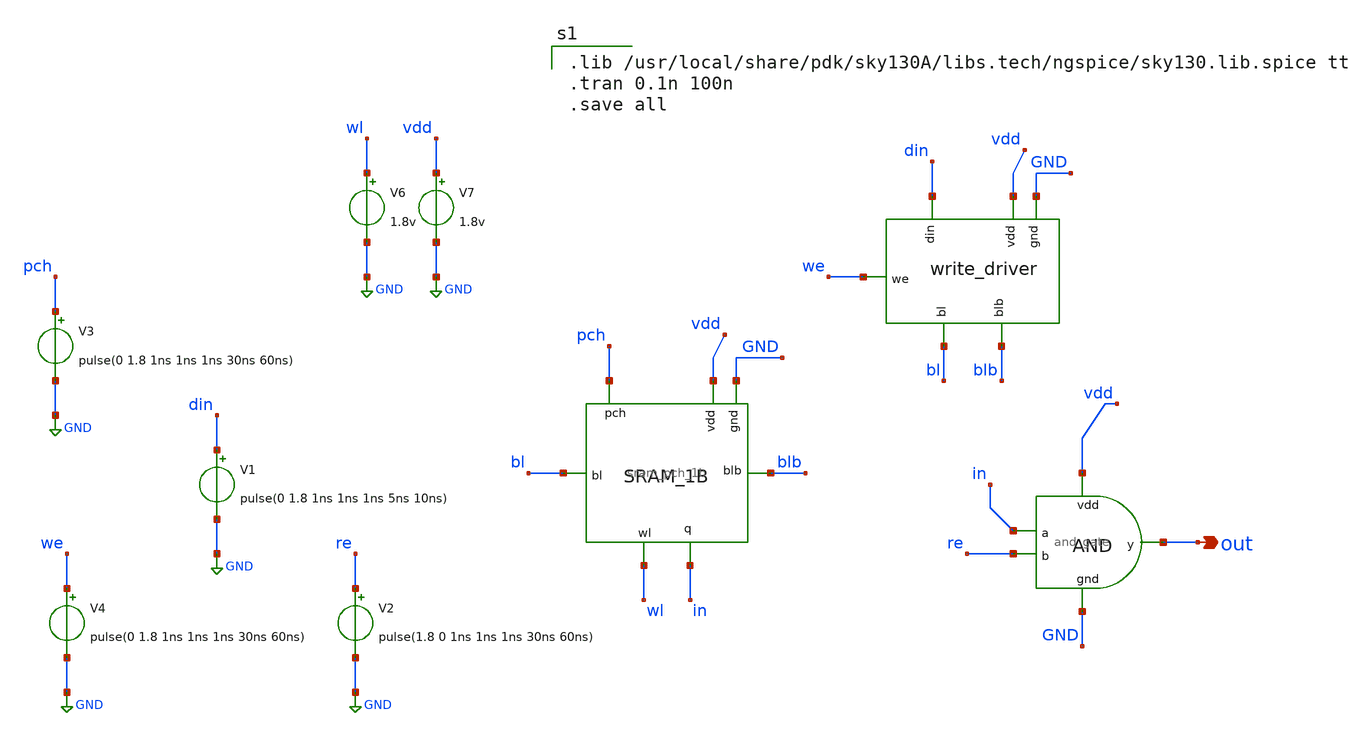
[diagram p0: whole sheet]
** sch_path: sram/sram1b_tb.sch
**.subckt sram1b_tb out
*.opin out
V1 din GND pulse(0 1.8 1ns 1ns 1ns 5ns 10ns)
V6 wl GND 1.8v
V7 vdd GND 1.8v
x2 vdd GND din bl blb we write_driver
x1 pch wl bl in GND vdd blb sram_pch_1b
V2 re GND pulse(1.8 0 1ns 1ns 1ns 30ns 60ns)
V4 we GND pulse(0 1.8 1ns 1ns 1ns 30ns 60ns)
V3 pch GND pulse(0 1.8 1ns 1ns 1ns 30ns 60ns)
x3 vdd in out re GND and_gate
**** begin user architecture code

.lib /usr/local/share/pdk/sky130A/libs.tech/ngspice/sky130.lib.spice tt
.tran 0.1n 100n
.save all

**** end user architecture code
**.ends

* expanding   symbol:  write_driver.sym # of pins=6
** sym_path: sram/write_driver.sym
** sch_path: sram/write_driver.sch
.subckt write_driver vdd gnd din bl blb we
*.ipin din
*.ipin we
*.opin bl
*.opin blb
*.ipin vdd
*.ipin gnd
XM1 net2 web vdd vdd sky130_fd_pr__pfet_01v8 L=0.15 W=1 nf=1 ad='int((nf+1)/2) * W/nf * 0.29' as='int((nf+2)/2) * W/nf * 0.29'
+ pd='2*int((nf+1)/2) * (W/nf + 0.29)' ps='2*int((nf+2)/2) * (W/nf + 0.29)' nrd='0.29 / W' nrs='0.29 / W'
+ sa=0 sb=0 sd=0 mult=1 m=1
XM2 blb din net1 blb sky130_fd_pr__nfet_01v8 L=0.15 W=1 nf=1 ad='int((nf+1)/2) * W/nf * 0.29' as='int((nf+2)/2) * W/nf * 0.29'
+ pd='2*int((nf+1)/2) * (W/nf + 0.29)' ps='2*int((nf+2)/2) * (W/nf + 0.29)' nrd='0.29 / W' nrs='0.29 / W'
+ sa=0 sb=0 sd=0 mult=1 m=1
XM3 blb din net2 net2 sky130_fd_pr__pfet_01v8 L=0.15 W=1 nf=1 ad='int((nf+1)/2) * W/nf * 0.29' as='int((nf+2)/2) * W/nf * 0.29'
+ pd='2*int((nf+1)/2) * (W/nf + 0.29)' ps='2*int((nf+2)/2) * (W/nf + 0.29)' nrd='0.29 / W' nrs='0.29 / W'
+ sa=0 sb=0 sd=0 mult=1 m=1
XM4 net1 we gnd net1 sky130_fd_pr__nfet_01v8 L=0.15 W=1 nf=1 ad='int((nf+1)/2) * W/nf * 0.29' as='int((nf+2)/2) * W/nf * 0.29'
+ pd='2*int((nf+1)/2) * (W/nf + 0.29)' ps='2*int((nf+2)/2) * (W/nf + 0.29)' nrd='0.29 / W' nrs='0.29 / W'
+ sa=0 sb=0 sd=0 mult=1 m=1
XM5 net4 web vdd vdd sky130_fd_pr__pfet_01v8 L=0.15 W=1 nf=1 ad='int((nf+1)/2) * W/nf * 0.29' as='int((nf+2)/2) * W/nf * 0.29'
+ pd='2*int((nf+1)/2) * (W/nf + 0.29)' ps='2*int((nf+2)/2) * (W/nf + 0.29)' nrd='0.29 / W' nrs='0.29 / W'
+ sa=0 sb=0 sd=0 mult=1 m=1
XM6 bl dinb net3 net3 sky130_fd_pr__nfet_01v8 L=0.15 W=1 nf=1 ad='int((nf+1)/2) * W/nf * 0.29' as='int((nf+2)/2) * W/nf * 0.29'
+ pd='2*int((nf+1)/2) * (W/nf + 0.29)' ps='2*int((nf+2)/2) * (W/nf + 0.29)' nrd='0.29 / W' nrs='0.29 / W'
+ sa=0 sb=0 sd=0 mult=1 m=1
XM7 bl dinb net4 net4 sky130_fd_pr__pfet_01v8 L=0.15 W=1 nf=1 ad='int((nf+1)/2) * W/nf * 0.29' as='int((nf+2)/2) * W/nf * 0.29'
+ pd='2*int((nf+1)/2) * (W/nf + 0.29)' ps='2*int((nf+2)/2) * (W/nf + 0.29)' nrd='0.29 / W' nrs='0.29 / W'
+ sa=0 sb=0 sd=0 mult=1 m=1
XM8 net3 we gnd gnd sky130_fd_pr__nfet_01v8 L=0.15 W=1 nf=1 ad='int((nf+1)/2) * W/nf * 0.29' as='int((nf+2)/2) * W/nf * 0.29'
+ pd='2*int((nf+1)/2) * (W/nf + 0.29)' ps='2*int((nf+2)/2) * (W/nf + 0.29)' nrd='0.29 / W' nrs='0.29 / W'
+ sa=0 sb=0 sd=0 mult=1 m=1
x1 vdd din dinb gnd inverter
x2 vdd we web gnd inverter
.ends


* expanding   symbol:  sram_pch_1b.sym # of pins=7
** sym_path: sram/sram_pch_1b.sym
** sch_path: sram/sram_pch_1b.sch
.subckt sram_pch_1b pch wl bl q gnd vdd blb
*.ipin gnd
*.ipin bl
*.ipin blb
*.ipin vdd
*.ipin wl
*.ipin pch
*.opin q
XM1 blb wl net1 gnd sky130_fd_pr__nfet_01v8 L=0.15 W=1 nf=1 ad='int((nf+1)/2) * W/nf * 0.29' as='int((nf+2)/2) * W/nf * 0.29'
+ pd='2*int((nf+1)/2) * (W/nf + 0.29)' ps='2*int((nf+2)/2) * (W/nf + 0.29)' nrd='0.29 / W' nrs='0.29 / W'
+ sa=0 sb=0 sd=0 mult=1 m=1
XM3 q wl bl gnd sky130_fd_pr__nfet_01v8 L=0.15 W=1 nf=1 ad='int((nf+1)/2) * W/nf * 0.29' as='int((nf+2)/2) * W/nf * 0.29'
+ pd='2*int((nf+1)/2) * (W/nf + 0.29)' ps='2*int((nf+2)/2) * (W/nf + 0.29)' nrd='0.29 / W' nrs='0.29 / W'
+ sa=0 sb=0 sd=0 mult=1 m=1
XM5 q net1 vdd vdd sky130_fd_pr__pfet_01v8 L=0.15 W=1 nf=1 ad='int((nf+1)/2) * W/nf * 0.29' as='int((nf+2)/2) * W/nf * 0.29'
+ pd='2*int((nf+1)/2) * (W/nf + 0.29)' ps='2*int((nf+2)/2) * (W/nf + 0.29)' nrd='0.29 / W' nrs='0.29 / W'
+ sa=0 sb=0 sd=0 mult=1 m=1
XM6 net1 q vdd vdd sky130_fd_pr__pfet_01v8 L=0.15 W=1 nf=1 ad='int((nf+1)/2) * W/nf * 0.29' as='int((nf+2)/2) * W/nf * 0.29'
+ pd='2*int((nf+1)/2) * (W/nf + 0.29)' ps='2*int((nf+2)/2) * (W/nf + 0.29)' nrd='0.29 / W' nrs='0.29 / W'
+ sa=0 sb=0 sd=0 mult=1 m=1
XM7 bl pch vdd vdd sky130_fd_pr__pfet_01v8 L=0.15 W=1 nf=1 ad='int((nf+1)/2) * W/nf * 0.29' as='int((nf+2)/2) * W/nf * 0.29'
+ pd='2*int((nf+1)/2) * (W/nf + 0.29)' ps='2*int((nf+2)/2) * (W/nf + 0.29)' nrd='0.29 / W' nrs='0.29 / W'
+ sa=0 sb=0 sd=0 mult=1 m=1
XM8 blb pch vdd vdd sky130_fd_pr__pfet_01v8 L=0.15 W=1 nf=1 ad='int((nf+1)/2) * W/nf * 0.29' as='int((nf+2)/2) * W/nf * 0.29'
+ pd='2*int((nf+1)/2) * (W/nf + 0.29)' ps='2*int((nf+2)/2) * (W/nf + 0.29)' nrd='0.29 / W' nrs='0.29 / W'
+ sa=0 sb=0 sd=0 mult=1 m=1
XM9 bl pch blb blb sky130_fd_pr__pfet_01v8 L=0.15 W=1 nf=1 ad='int((nf+1)/2) * W/nf * 0.29' as='int((nf+2)/2) * W/nf * 0.29'
+ pd='2*int((nf+1)/2) * (W/nf + 0.29)' ps='2*int((nf+2)/2) * (W/nf + 0.29)' nrd='0.29 / W' nrs='0.29 / W'
+ sa=0 sb=0 sd=0 mult=1 m=1
XM2 net1 q gnd gnd sky130_fd_pr__nfet_01v8 L=0.15 W=1 nf=1 ad='int((nf+1)/2) * W/nf * 0.29' as='int((nf+2)/2) * W/nf * 0.29'
+ pd='2*int((nf+1)/2) * (W/nf + 0.29)' ps='2*int((nf+2)/2) * (W/nf + 0.29)' nrd='0.29 / W' nrs='0.29 / W'
+ sa=0 sb=0 sd=0 mult=1 m=1
XM4 q net1 gnd gnd sky130_fd_pr__nfet_01v8 L=0.15 W=1 nf=1 ad='int((nf+1)/2) * W/nf * 0.29' as='int((nf+2)/2) * W/nf * 0.29'
+ pd='2*int((nf+1)/2) * (W/nf + 0.29)' ps='2*int((nf+2)/2) * (W/nf + 0.29)' nrd='0.29 / W' nrs='0.29 / W'
+ sa=0 sb=0 sd=0 mult=1 m=1
.ends


* expanding   symbol:  and_gate.sym # of pins=5
** sym_path: sram/and_gate.sym
** sch_path: sram/and_gate.sch
.subckt and_gate vdd a y b gnd
*.ipin a
*.ipin b
*.ipin vdd
*.ipin gnd
*.opin y
x2 vdd net1 y gnd inverter
x1 vdd a b gnd net1 nand_gate
.ends


* expanding   symbol:  inverter.sym # of pins=4
** sym_path: sram/inverter.sym
** sch_path: sram/inverter.sch
.subckt inverter vdd vin vout gnd
*.ipin vin
*.ipin vdd
*.ipin gnd
*.opin vout
XM1 vout vin gnd gnd sky130_fd_pr__nfet_01v8 L=0.15 W=1 nf=1 ad='int((nf+1)/2) * W/nf * 0.29' as='int((nf+2)/2) * W/nf * 0.29'
+ pd='2*int((nf+1)/2) * (W/nf + 0.29)' ps='2*int((nf+2)/2) * (W/nf + 0.29)' nrd='0.29 / W' nrs='0.29 / W'
+ sa=0 sb=0 sd=0 mult=1 m=1
XM2 vout vin vdd vdd sky130_fd_pr__pfet_01v8 L=0.15 W=1 nf=1 ad='int((nf+1)/2) * W/nf * 0.29' as='int((nf+2)/2) * W/nf * 0.29'
+ pd='2*int((nf+1)/2) * (W/nf + 0.29)' ps='2*int((nf+2)/2) * (W/nf + 0.29)' nrd='0.29 / W' nrs='0.29 / W'
+ sa=0 sb=0 sd=0 mult=1 m=1
.ends


* expanding   symbol:  nand_gate.sym # of pins=5
** sym_path: sram/nand_gate.sym
** sch_path: sram/nand_gate.sch
.subckt nand_gate vdd a b gnd y
*.ipin a
*.ipin b
*.ipin vdd
*.ipin gnd
*.opin y
XM1 y a vdd vdd sky130_fd_pr__pfet_01v8 L=0.15 W=1 nf=1 ad='int((nf+1)/2) * W/nf * 0.29' as='int((nf+2)/2) * W/nf * 0.29'
+ pd='2*int((nf+1)/2) * (W/nf + 0.29)' ps='2*int((nf+2)/2) * (W/nf + 0.29)' nrd='0.29 / W' nrs='0.29 / W'
+ sa=0 sb=0 sd=0 mult=1 m=1
XM2 y a net1 net1 sky130_fd_pr__nfet_01v8 L=0.15 W=1 nf=1 ad='int((nf+1)/2) * W/nf * 0.29' as='int((nf+2)/2) * W/nf * 0.29'
+ pd='2*int((nf+1)/2) * (W/nf + 0.29)' ps='2*int((nf+2)/2) * (W/nf + 0.29)' nrd='0.29 / W' nrs='0.29 / W'
+ sa=0 sb=0 sd=0 mult=1 m=1
XM3 y b vdd vdd sky130_fd_pr__pfet_01v8 L=0.15 W=1 nf=1 ad='int((nf+1)/2) * W/nf * 0.29' as='int((nf+2)/2) * W/nf * 0.29'
+ pd='2*int((nf+1)/2) * (W/nf + 0.29)' ps='2*int((nf+2)/2) * (W/nf + 0.29)' nrd='0.29 / W' nrs='0.29 / W'
+ sa=0 sb=0 sd=0 mult=1 m=1
XM4 net1 b gnd gnd sky130_fd_pr__nfet_01v8 L=0.15 W=1 nf=1 ad='int((nf+1)/2) * W/nf * 0.29' as='int((nf+2)/2) * W/nf * 0.29'
+ pd='2*int((nf+1)/2) * (W/nf + 0.29)' ps='2*int((nf+2)/2) * (W/nf + 0.29)' nrd='0.29 / W' nrs='0.29 / W'
+ sa=0 sb=0 sd=0 mult=1 m=1
.ends

.GLOBAL GND
.end
